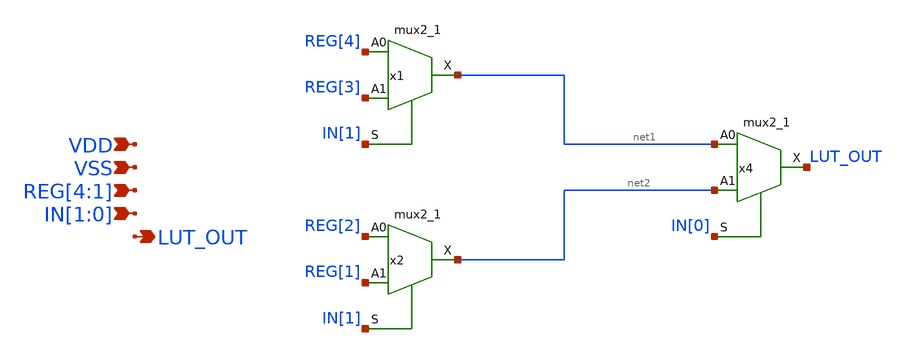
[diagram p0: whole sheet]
** sch_path: designs/libs/core_fpga/LUT/LUT.sch
**.subckt LUT REG[4],REG[3],REG[2],REG[1] IN[1],IN[0] LUT_OUT VDD VSS
*.ipin REG[4],REG[3],REG[2],REG[1]
*.ipin IN[1],IN[0]
*.opin LUT_OUT
*.ipin VDD
*.ipin VSS
x1 REG[4] REG[3] IN[1] VSS VDD VSS VDD net1 gf180mcu_fd_sc_mcu9t5v0__mux2_1
x2 REG[2] REG[1] IN[1] VSS VDD VSS VDD net2 gf180mcu_fd_sc_mcu9t5v0__mux2_1
x4 net1 net2 IN[0] VSS VDD VSS VDD LUT_OUT gf180mcu_fd_sc_mcu9t5v0__mux2_1
**.ends
.end
